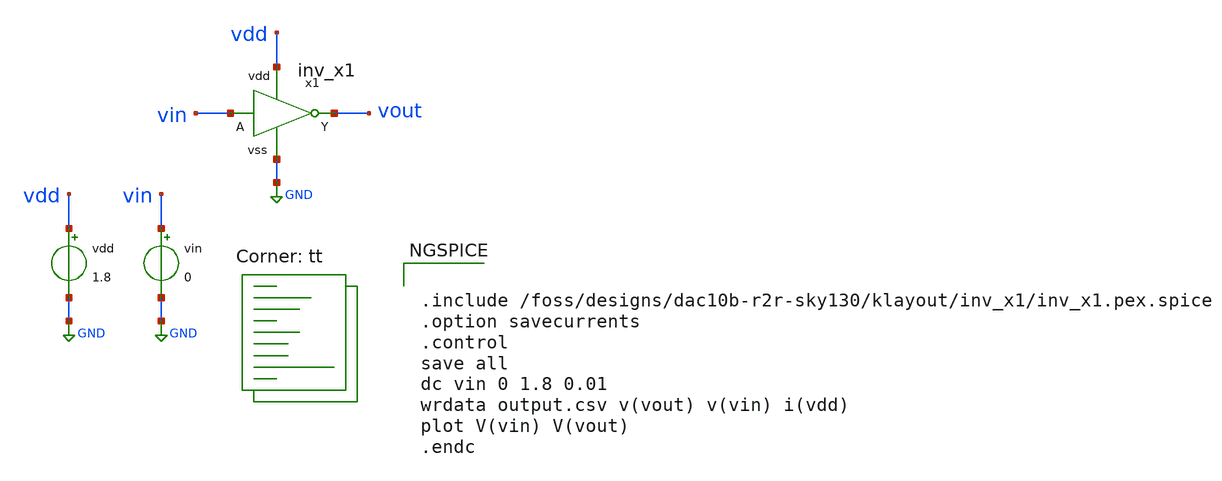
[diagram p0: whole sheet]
** sch_path: xschem/inv_x1/inv_x1_tb.sch
**.subckt inv_x1_tb
x1 vdd vout vin GND inv_x1
vdd vdd GND 1.8
vin vin GND 0
**** begin user architecture code
.lib $::SKYWATER_MODELS/sky130.lib.spice tt


.include /foss/designs/dac10b-r2r-sky130/klayout/inv_x1/inv_x1.pex.spice
.option savecurrents
.control
save all
dc vin 0 1.8 0.01
wrdata output.csv v(vout) v(vin) i(vdd)
plot V(vin) V(vout)
.endc


**** end user architecture code
**.ends
.GLOBAL GND
.end
